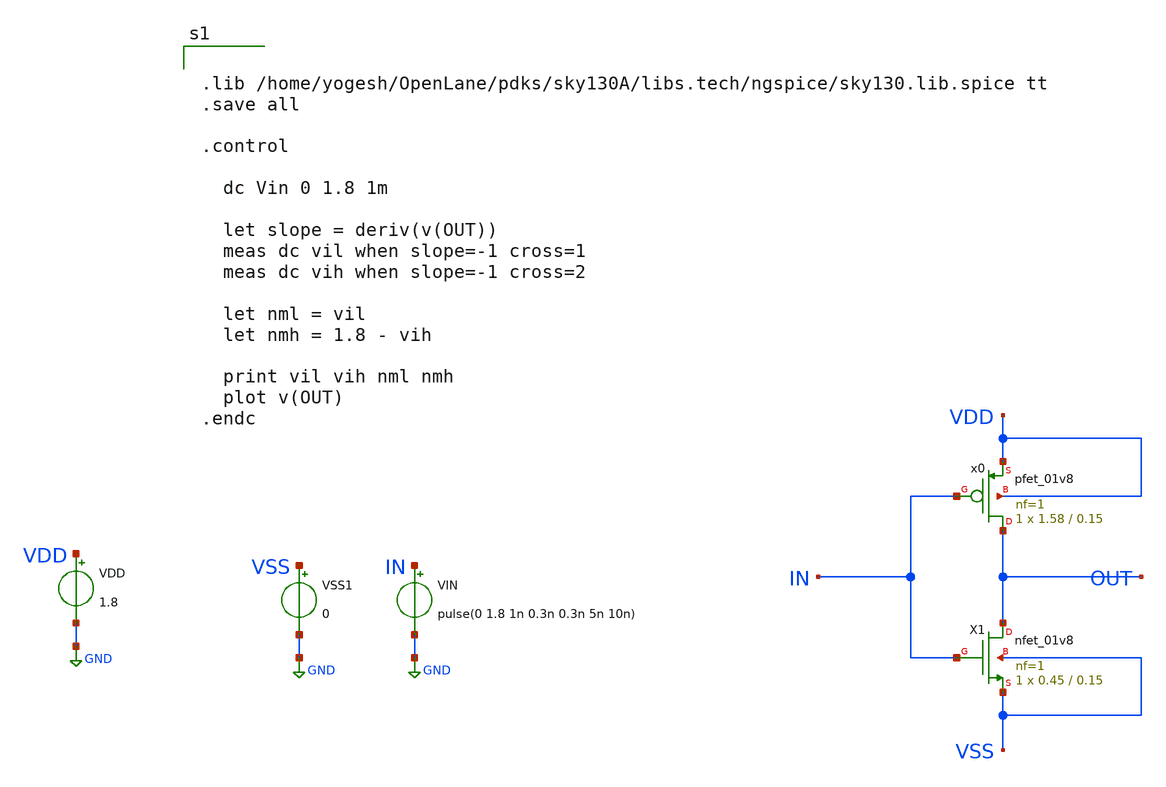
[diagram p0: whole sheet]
** sch_path: OneDrive/Documents/CMOS-Inverter-Design-and-Analysis-using-Sky130pdk-main/xschem/INV_cmos_ nse.sch
**.subckt INV_cmos_ nse
XX1 OUT IN VSS VSS sky130_fd_pr__nfet_01v8 L=0.15 W=0.45 nf=1 ad='int((nf+1)/2) * W/nf * 0.29' as='int((nf+2)/2) * W/nf * 0.29'
+ pd='2*int((nf+1)/2) * (W/nf + 0.29)' ps='2*int((nf+2)/2) * (W/nf + 0.29)' nrd='0.29 / W' nrs='0.29 / W'
+ sa=0 sb=0 sd=0 mult=1 m=1
VIN IN GND pulse(0 1.8 1n 0.3n 0.3n 5n 10n)
VSS1 VSS GND 0
VDD VDD GND 1.8
Xx0 OUT IN VDD VDD sky130_fd_pr__pfet_01v8 L=0.15 W=1.58 nf=1 ad='int((nf+1)/2) * W/nf * 0.29' as='int((nf+2)/2) * W/nf * 0.29'
+ pd='2*int((nf+1)/2) * (W/nf + 0.29)' ps='2*int((nf+2)/2) * (W/nf + 0.29)' nrd='0.29 / W' nrs='0.29 / W'
+ sa=0 sb=0 sd=0 mult=1 m=1
**** begin user architecture code


.lib /home/yogesh/OpenLane/pdks/sky130A/libs.tech/ngspice/sky130.lib.spice tt
.save all

.control

  dc Vin 0 1.8 1m

  let slope = deriv(v(OUT))
  meas dc vil when slope=-1 cross=1
  meas dc vih when slope=-1 cross=2

  let nml = vil
  let nmh = 1.8 - vih

  print vil vih nml nmh
  plot v(OUT)
.endc

**** end user architecture code
**.ends
.GLOBAL GND
.end
